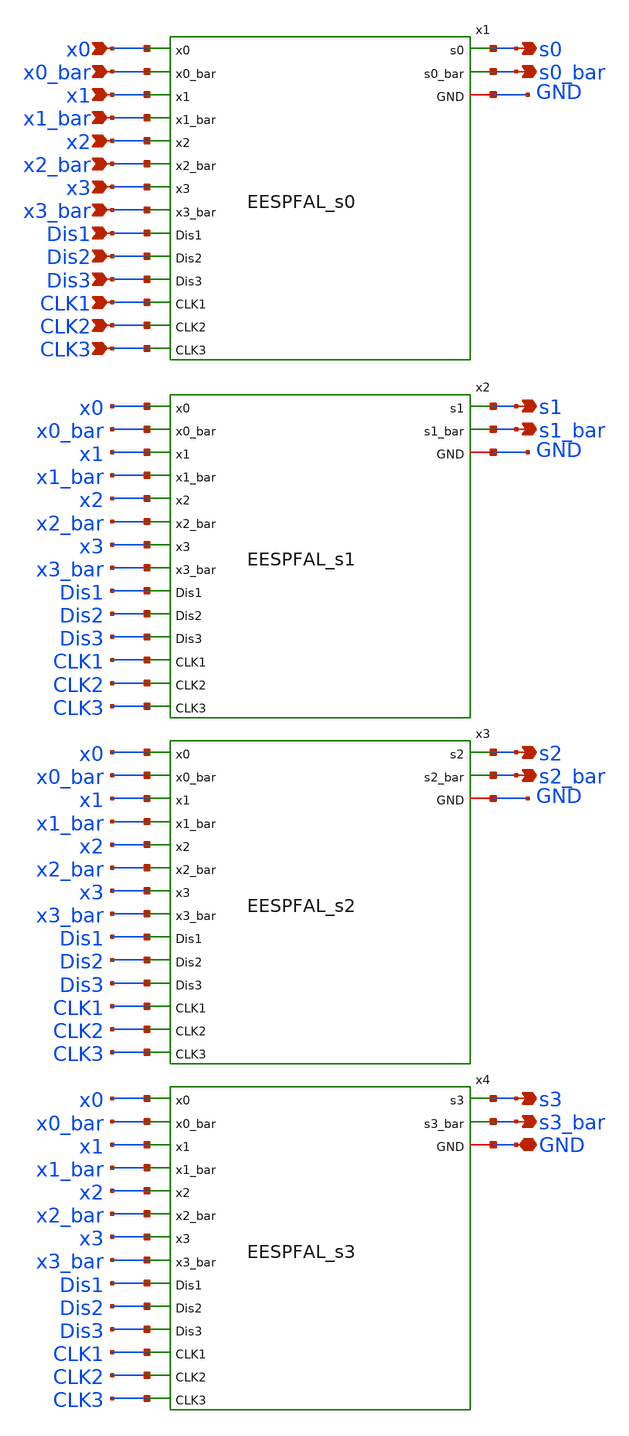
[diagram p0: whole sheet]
** sch_path: skywater_stuff/EESPFAL_Sbox_flat.sch
**.subckt EESPFAL_Sbox_flat GND x0 x0_bar x1 x1_bar x2 x2_bar x3 x3_bar Dis1 Dis2 Dis3 s0 s0_bar
*+ s1_bar s1 s2 s2_bar s3_bar s3 CLK1 CLK2 CLK3
*.iopin GND
*.ipin x0
*.ipin x0_bar
*.ipin x1
*.ipin x1_bar
*.ipin x2
*.ipin x2_bar
*.ipin x3
*.ipin x3_bar
*.ipin Dis1
*.ipin Dis2
*.ipin Dis3
*.opin s0
*.opin s0_bar
*.opin s1_bar
*.opin s1
*.opin s2
*.opin s2_bar
*.opin s3_bar
*.opin s3
*.ipin CLK1
*.ipin CLK2
*.ipin CLK3
x4 GND x0 x0_bar x1 x1_bar x2 x2_bar x3 x3_bar s3_bar CLK1 s3 Dis1 Dis3 CLK3 Dis2 CLK2 EESPFAL_s3
x2 GND x0 x0_bar x1 x1_bar x2 x2_bar x3 x3_bar s1_bar s1 CLK1 Dis1 Dis3 CLK3 Dis2 CLK2 EESPFAL_s1
x3 GND x0 x0_bar x1 x1_bar x2 x2_bar x3 x3_bar CLK1 Dis1 Dis3 Dis2 CLK3 CLK2 s2_bar s2 EESPFAL_s2
x1 GND x0 x0_bar x1 x1_bar x2 x2_bar x3 x3_bar CLK1 Dis1 CLK3 Dis2 CLK2 Dis3 s0 s0_bar EESPFAL_s0
**.ends
.end
